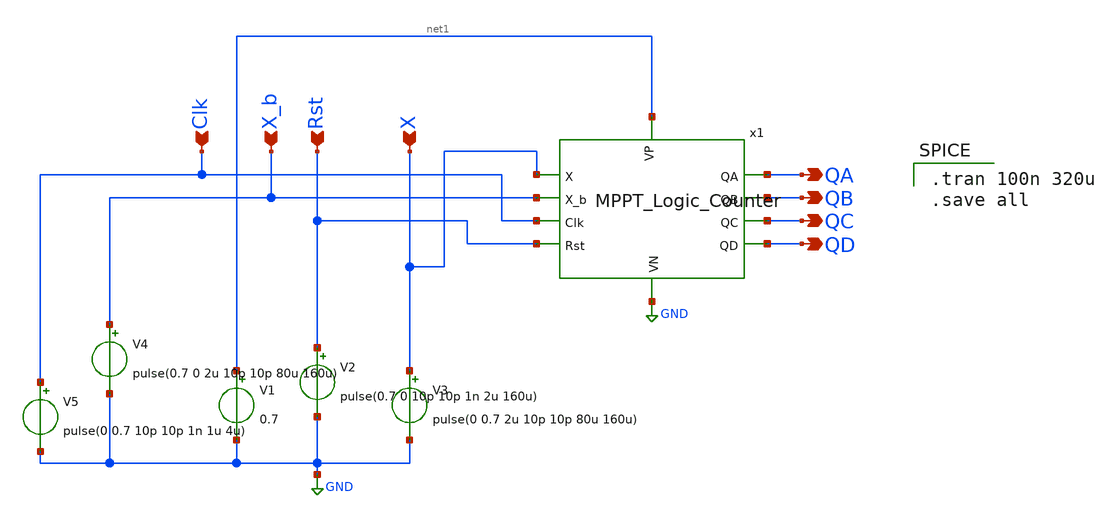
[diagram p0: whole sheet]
** sch_path: Blocks/MPPT/MPPT_Logic_Counter_test.sch
**.subckt MPPT_Logic_Counter_test QA Clk X_b Rst X QD QC QB
*.opin QA
*.ipin Clk
*.ipin X_b
*.ipin Rst
*.ipin X
*.opin QD
*.opin QC
*.opin QB
V2 Rst GND pulse(0.7 0 10p 10p 1n 2u 160u)
V4 X_b GND pulse(0.7 0 2u 10p 10p 80u 160u)
V5 Clk GND pulse(0 0.7 10p 10p 1n 1u 4u)
V3 X GND pulse(0 0.7 2u 10p 10p 80u 160u)
V1 net1 GND 0.7
x1 QA Clk X_b Rst GND X net1 QD QB QC MPPT_Logic_Counter
**** begin user architecture code

** opencircuitdesign pdks install
.lib $::SKYWATER_MODELS/sky130.lib.spice tt



.tran 100n 320u
.save all

**** end user architecture code
**.ends

* expanding   symbol:  pico_chipathon/Blocks/MPPT/MPPT_Logic_Counter.sym # of pins=10
** sym_path: Blocks/MPPT/MPPT_Logic_Counter.sym
** sch_path: Blocks/MPPT/MPPT_Logic_Counter.sch
.subckt MPPT_Logic_Counter QA Clk X_b Rst VN X VP QD QB QC
*.opin QD
*.ipin VP
*.opin QC
*.opin QB
*.opin QA
*.ipin VN
*.ipin X
*.ipin X_b
*.ipin Clk
*.ipin Rst
x4 net47 net46 net2 VP VN NAND
x5 QD X_b net38 VP VN NAND
x6 net51 net50 net3 VP VN NAND
x16 QA QD net29 VP VN NAND
x48 QB QD net31 VP VN NAND
x49 QC QD net32 VP VN NAND
x50 QD X net35 VP VN NAND
x52 net44 net43 net28 VP VN NAND
x54 VP net14 X_b QC QB_b QA_b VN nand4
x12 VP net15 X_b QD QB_b QA_b VN nand4
x15 VP net17 QD QC QB QA VN nand4
x22 VP net8 X QC_b QB QA VN nand4
x24 VP net36 X QC QB QA VN nand4
x17 VP net52 net53 net57 net50 VN nor3
x26 VP net54 net55 net56 net51 VN nor3
x56 VP net10 net11 net48 net46 VN nor3
x57 VP net49 net16 net18 net47 VN nor3
x25 VP net30 net33 net45 net43 VN nor3
x64 X_b QB QA VP VN net9 NAND3
x9 X QB_b QA VP VN net12 NAND3
x10 X QB QA_b VP VN net13 NAND3
x11 X_b QC QA VP VN net4 NAND3
x13 QC QB QA_b VP VN net5 NAND3
x14 QD QC QA VP VN net6 NAND3
x19 X QC QB_b VP VN net7 NAND3
x20 QC_b QB_b QA_b VP VN net39 NAND3
x23 VP net34 net37 net44 VN NOR2
x8 VP net38 net39 net56 VN NOR2
x1 net2 Clk Rst VN VP QB QB_b DFF1
x18 net3 Clk Rst VN VP QC QC_b DFF1
x29 net28 Clk Rst VN VP QD DFF
x32 net17 net18 VP VN INV
x38 net15 net16 VP VN INV
x39 net14 net49 VP VN INV
x40 net13 net48 VP VN INV
x42 net9 net10 VP VN INV
x43 net12 net11 VP VN INV
x31 net8 net55 VP VN INV
x33 net7 net54 VP VN INV
x36 net6 net57 VP VN INV
x37 net5 net53 VP VN INV
x41 net4 net52 VP VN INV
x34 net29 net30 VP VN INV
x44 net31 net33 VP VN INV
x51 net32 net45 VP VN INV
x53 net35 net34 VP VN INV
x55 net36 net37 VP VN INV
x35 net1 Clk Rst VN VP QA QA_b DFF1
x58 VP net20 net23 net42 net40 VN nor3
x59 VP net40 net41 net1 VN NOR2
x3 net27 net24 net41 VP VN NAND
x21 net19 net20 VP VN INV
x27 net21 net23 VP VN INV
x28 net22 net42 VP VN INV
x30 net25 net24 VP VN INV
x2 net26 net27 VP VN INV
x60 VP net26 X QD QC QB VN nand4
x7 QA_b QB net19 VP VN NAND
x45 QA_b QC net21 VP VN NAND
x46 QA_b QD net22 VP VN NAND
x47 QA_b X net25 VP VN NAND
.ends


* expanding   symbol:  pico_chipathon/component/NAND2/NAND.sym # of pins=5
** sym_path: component/NAND2/NAND.sym
** sch_path: component/NAND2/NAND.sch
.subckt NAND B A Y VP VN
*.iopin VP
*.ipin A
*.ipin B
*.opin Y
*.iopin VN
XM1 Y A VP VP sky130_fd_pr__pfet_01v8 L=0.15 W=1.26 nf=1 ad='int((nf+1)/2) * W/nf * 0.29' as='int((nf+2)/2) * W/nf * 0.29'
+ pd='2*int((nf+1)/2) * (W/nf + 0.29)' ps='2*int((nf+2)/2) * (W/nf + 0.29)' nrd='0.29 / W' nrs='0.29 / W'
+ sa=0 sb=0 sd=0 mult=1 m=1
XM2 Y B VP VP sky130_fd_pr__pfet_01v8 L=0.15 W=1.26 nf=1 ad='int((nf+1)/2) * W/nf * 0.29' as='int((nf+2)/2) * W/nf * 0.29'
+ pd='2*int((nf+1)/2) * (W/nf + 0.29)' ps='2*int((nf+2)/2) * (W/nf + 0.29)' nrd='0.29 / W' nrs='0.29 / W'
+ sa=0 sb=0 sd=0 mult=1 m=1
XM3 Y A net1 net1 sky130_fd_pr__nfet_01v8 L=0.15 W=0.84 nf=1 ad='int((nf+1)/2) * W/nf * 0.29' as='int((nf+2)/2) * W/nf * 0.29'
+ pd='2*int((nf+1)/2) * (W/nf + 0.29)' ps='2*int((nf+2)/2) * (W/nf + 0.29)' nrd='0.29 / W' nrs='0.29 / W'
+ sa=0 sb=0 sd=0 mult=1 m=1
XM4 net1 B VN VN sky130_fd_pr__nfet_01v8 L=0.15 W=0.84 nf=1 ad='int((nf+1)/2) * W/nf * 0.29' as='int((nf+2)/2) * W/nf * 0.29'
+ pd='2*int((nf+1)/2) * (W/nf + 0.29)' ps='2*int((nf+2)/2) * (W/nf + 0.29)' nrd='0.29 / W' nrs='0.29 / W'
+ sa=0 sb=0 sd=0 mult=1 m=1
.ends


* expanding   symbol:  pico_chipathon/component/NAND4/nand4.sym # of pins=7
** sym_path: component/NAND4/nand4.sym
** sch_path: component/NAND4/nand4.sch
.subckt nand4 VP Y A B C D VN
*.ipin A
*.ipin B
*.ipin C
*.opin Y
*.ipin D
*.ipin VP
*.ipin VN
XM1 Y A net1 VN sky130_fd_pr__nfet_01v8 L=0.15 W=1.68 nf=1 ad='int((nf+1)/2) * W/nf * 0.29' as='int((nf+2)/2) * W/nf * 0.29'
+ pd='2*int((nf+1)/2) * (W/nf + 0.29)' ps='2*int((nf+2)/2) * (W/nf + 0.29)' nrd='0.29 / W' nrs='0.29 / W'
+ sa=0 sb=0 sd=0 mult=1 m=1
XM2 net1 B net2 VN sky130_fd_pr__nfet_01v8 L=0.15 W=1.68 nf=1 ad='int((nf+1)/2) * W/nf * 0.29' as='int((nf+2)/2) * W/nf * 0.29'
+ pd='2*int((nf+1)/2) * (W/nf + 0.29)' ps='2*int((nf+2)/2) * (W/nf + 0.29)' nrd='0.29 / W' nrs='0.29 / W'
+ sa=0 sb=0 sd=0 mult=1 m=1
XM3 net2 C net3 VN sky130_fd_pr__nfet_01v8 L=0.15 W=1.68 nf=1 ad='int((nf+1)/2) * W/nf * 0.29' as='int((nf+2)/2) * W/nf * 0.29'
+ pd='2*int((nf+1)/2) * (W/nf + 0.29)' ps='2*int((nf+2)/2) * (W/nf + 0.29)' nrd='0.29 / W' nrs='0.29 / W'
+ sa=0 sb=0 sd=0 mult=1 m=1
XM4 Y A VP VP sky130_fd_pr__pfet_01v8 L=0.15 W=1.26 nf=1 ad='int((nf+1)/2) * W/nf * 0.29' as='int((nf+2)/2) * W/nf * 0.29'
+ pd='2*int((nf+1)/2) * (W/nf + 0.29)' ps='2*int((nf+2)/2) * (W/nf + 0.29)' nrd='0.29 / W' nrs='0.29 / W'
+ sa=0 sb=0 sd=0 mult=1 m=1
XM5 Y B VP VP sky130_fd_pr__pfet_01v8 L=0.15 W=1.26 nf=1 ad='int((nf+1)/2) * W/nf * 0.29' as='int((nf+2)/2) * W/nf * 0.29'
+ pd='2*int((nf+1)/2) * (W/nf + 0.29)' ps='2*int((nf+2)/2) * (W/nf + 0.29)' nrd='0.29 / W' nrs='0.29 / W'
+ sa=0 sb=0 sd=0 mult=1 m=1
XM6 Y C VP VP sky130_fd_pr__pfet_01v8 L=0.15 W=1.26 nf=1 ad='int((nf+1)/2) * W/nf * 0.29' as='int((nf+2)/2) * W/nf * 0.29'
+ pd='2*int((nf+1)/2) * (W/nf + 0.29)' ps='2*int((nf+2)/2) * (W/nf + 0.29)' nrd='0.29 / W' nrs='0.29 / W'
+ sa=0 sb=0 sd=0 mult=1 m=1
XM7 Y D VP VP sky130_fd_pr__pfet_01v8 L=0.15 W=1.26 nf=1 ad='int((nf+1)/2) * W/nf * 0.29' as='int((nf+2)/2) * W/nf * 0.29'
+ pd='2*int((nf+1)/2) * (W/nf + 0.29)' ps='2*int((nf+2)/2) * (W/nf + 0.29)' nrd='0.29 / W' nrs='0.29 / W'
+ sa=0 sb=0 sd=0 mult=1 m=1
XM8 net3 D VN VN sky130_fd_pr__nfet_01v8 L=0.15 W=1.68 nf=1 ad='int((nf+1)/2) * W/nf * 0.29' as='int((nf+2)/2) * W/nf * 0.29'
+ pd='2*int((nf+1)/2) * (W/nf + 0.29)' ps='2*int((nf+2)/2) * (W/nf + 0.29)' nrd='0.29 / W' nrs='0.29 / W'
+ sa=0 sb=0 sd=0 mult=1 m=1
.ends


* expanding   symbol:  pico_chipathon/component/NOR3/nor3.sym # of pins=6
** sym_path: component/NOR3/nor3.sym
** sch_path: component/NOR3/nor3.sch
.subckt nor3 VP A B C Y VN
*.opin Y
*.ipin C
*.ipin A
*.ipin B
*.ipin VP
*.ipin VN
XM5 Y B VN VN sky130_fd_pr__nfet_01v8 L=0.15 W=0.42 nf=1 ad='int((nf+1)/2) * W/nf * 0.29' as='int((nf+2)/2) * W/nf * 0.29'
+ pd='2*int((nf+1)/2) * (W/nf + 0.29)' ps='2*int((nf+2)/2) * (W/nf + 0.29)' nrd='0.29 / W' nrs='0.29 / W'
+ sa=0 sb=0 sd=0 mult=1 m=1
XM3 Y A VN VN sky130_fd_pr__nfet_01v8 L=0.15 W=0.42 nf=1 ad='int((nf+1)/2) * W/nf * 0.29' as='int((nf+2)/2) * W/nf * 0.29'
+ pd='2*int((nf+1)/2) * (W/nf + 0.29)' ps='2*int((nf+2)/2) * (W/nf + 0.29)' nrd='0.29 / W' nrs='0.29 / W'
+ sa=0 sb=0 sd=0 mult=1 m=1
XM2 Y C net2 VP sky130_fd_pr__pfet_01v8 L=0.15 W=3.78 nf=1 ad='int((nf+1)/2) * W/nf * 0.29' as='int((nf+2)/2) * W/nf * 0.29'
+ pd='2*int((nf+1)/2) * (W/nf + 0.29)' ps='2*int((nf+2)/2) * (W/nf + 0.29)' nrd='0.29 / W' nrs='0.29 / W'
+ sa=0 sb=0 sd=0 mult=1 m=1
XM1 net1 A VP VP sky130_fd_pr__pfet_01v8 L=0.15 W=3.78 nf=1 ad='int((nf+1)/2) * W/nf * 0.29' as='int((nf+2)/2) * W/nf * 0.29'
+ pd='2*int((nf+1)/2) * (W/nf + 0.29)' ps='2*int((nf+2)/2) * (W/nf + 0.29)' nrd='0.29 / W' nrs='0.29 / W'
+ sa=0 sb=0 sd=0 mult=1 m=1
XM6 net2 B net1 VP sky130_fd_pr__pfet_01v8 L=0.15 W=3.78 nf=1 ad='int((nf+1)/2) * W/nf * 0.29' as='int((nf+2)/2) * W/nf * 0.29'
+ pd='2*int((nf+1)/2) * (W/nf + 0.29)' ps='2*int((nf+2)/2) * (W/nf + 0.29)' nrd='0.29 / W' nrs='0.29 / W'
+ sa=0 sb=0 sd=0 mult=1 m=1
XM8 Y C VN VN sky130_fd_pr__nfet_01v8 L=0.15 W=0.42 nf=1 ad='int((nf+1)/2) * W/nf * 0.29' as='int((nf+2)/2) * W/nf * 0.29'
+ pd='2*int((nf+1)/2) * (W/nf + 0.29)' ps='2*int((nf+2)/2) * (W/nf + 0.29)' nrd='0.29 / W' nrs='0.29 / W'
+ sa=0 sb=0 sd=0 mult=1 m=1
.ends


* expanding   symbol:  pico_chipathon/component/NAND3/NAND3.sym # of pins=6
** sym_path: component/NAND3/NAND3.sym
** sch_path: component/NAND3/NAND3.sch
.subckt NAND3 A B C VP VN Y
*.iopin VP
*.iopin VN
*.ipin A
*.ipin B
*.ipin C
*.opin Y
XM1 Y A net1 VN sky130_fd_pr__nfet_01v8 L=0.15 W=1.26 nf=1 ad='int((nf+1)/2) * W/nf * 0.29' as='int((nf+2)/2) * W/nf * 0.29'
+ pd='2*int((nf+1)/2) * (W/nf + 0.29)' ps='2*int((nf+2)/2) * (W/nf + 0.29)' nrd='0.29 / W' nrs='0.29 / W'
+ sa=0 sb=0 sd=0 mult=1 m=1
XM2 net1 B net2 VN sky130_fd_pr__nfet_01v8 L=0.15 W=1.26 nf=1 ad='int((nf+1)/2) * W/nf * 0.29' as='int((nf+2)/2) * W/nf * 0.29'
+ pd='2*int((nf+1)/2) * (W/nf + 0.29)' ps='2*int((nf+2)/2) * (W/nf + 0.29)' nrd='0.29 / W' nrs='0.29 / W'
+ sa=0 sb=0 sd=0 mult=1 m=1
XM3 net2 C VN VN sky130_fd_pr__nfet_01v8 L=0.15 W=1.26 nf=1 ad='int((nf+1)/2) * W/nf * 0.29' as='int((nf+2)/2) * W/nf * 0.29'
+ pd='2*int((nf+1)/2) * (W/nf + 0.29)' ps='2*int((nf+2)/2) * (W/nf + 0.29)' nrd='0.29 / W' nrs='0.29 / W'
+ sa=0 sb=0 sd=0 mult=1 m=1
XM4 Y A VP VP sky130_fd_pr__pfet_01v8 L=0.15 W=1.26 nf=1 ad='int((nf+1)/2) * W/nf * 0.29' as='int((nf+2)/2) * W/nf * 0.29'
+ pd='2*int((nf+1)/2) * (W/nf + 0.29)' ps='2*int((nf+2)/2) * (W/nf + 0.29)' nrd='0.29 / W' nrs='0.29 / W'
+ sa=0 sb=0 sd=0 mult=1 m=1
XM5 Y B VP VP sky130_fd_pr__pfet_01v8 L=0.15 W=1.26 nf=1 ad='int((nf+1)/2) * W/nf * 0.29' as='int((nf+2)/2) * W/nf * 0.29'
+ pd='2*int((nf+1)/2) * (W/nf + 0.29)' ps='2*int((nf+2)/2) * (W/nf + 0.29)' nrd='0.29 / W' nrs='0.29 / W'
+ sa=0 sb=0 sd=0 mult=1 m=1
XM6 Y C VP VP sky130_fd_pr__pfet_01v8 L=0.15 W=1.26 nf=1 ad='int((nf+1)/2) * W/nf * 0.29' as='int((nf+2)/2) * W/nf * 0.29'
+ pd='2*int((nf+1)/2) * (W/nf + 0.29)' ps='2*int((nf+2)/2) * (W/nf + 0.29)' nrd='0.29 / W' nrs='0.29 / W'
+ sa=0 sb=0 sd=0 mult=1 m=1
.ends


* expanding   symbol:  pico_chipathon/component/NOR2/NOR2.sym # of pins=5
** sym_path: component/NOR2/NOR2.sym
** sch_path: component/NOR2/NOR2.sch
.subckt NOR2 VP A B Y VN
*.opin Y
*.ipin A
*.ipin B
*.ipin VP
*.ipin VN
XM5 Y B VN VN sky130_fd_pr__nfet_01v8 L=0.15 W=0.42 nf=1 ad='int((nf+1)/2) * W/nf * 0.29' as='int((nf+2)/2) * W/nf * 0.29'
+ pd='2*int((nf+1)/2) * (W/nf + 0.29)' ps='2*int((nf+2)/2) * (W/nf + 0.29)' nrd='0.29 / W' nrs='0.29 / W'
+ sa=0 sb=0 sd=0 mult=1 m=1
XM3 Y A VN VN sky130_fd_pr__nfet_01v8 L=0.15 W=0.42 nf=1 ad='int((nf+1)/2) * W/nf * 0.29' as='int((nf+2)/2) * W/nf * 0.29'
+ pd='2*int((nf+1)/2) * (W/nf + 0.29)' ps='2*int((nf+2)/2) * (W/nf + 0.29)' nrd='0.29 / W' nrs='0.29 / W'
+ sa=0 sb=0 sd=0 mult=1 m=1
XM2 net1 A VP VP sky130_fd_pr__pfet_01v8 L=0.15 W=2.52 nf=1 ad='int((nf+1)/2) * W/nf * 0.29' as='int((nf+2)/2) * W/nf * 0.29'
+ pd='2*int((nf+1)/2) * (W/nf + 0.29)' ps='2*int((nf+2)/2) * (W/nf + 0.29)' nrd='0.29 / W' nrs='0.29 / W'
+ sa=0 sb=0 sd=0 mult=1 m=1
XM4 Y B net1 VP sky130_fd_pr__pfet_01v8 L=0.15 W=2.52 nf=1 ad='int((nf+1)/2) * W/nf * 0.29' as='int((nf+2)/2) * W/nf * 0.29'
+ pd='2*int((nf+1)/2) * (W/nf + 0.29)' ps='2*int((nf+2)/2) * (W/nf + 0.29)' nrd='0.29 / W' nrs='0.29 / W'
+ sa=0 sb=0 sd=0 mult=1 m=1
.ends


* expanding   symbol:  pico_chipathon/component/FlipFlops/DFF1.sym # of pins=7
** sym_path: component/FlipFlops/DFF1.sym
** sch_path: component/FlipFlops/DFF1.sch
.subckt DFF1 D Clk RST VN VP Q Qb
*.opin Q
*.iopin VN
*.iopin VP
*.ipin Clk
*.ipin D
*.ipin RST
*.opin Qb
x7 net2 net4 net3 VP VN NAND
x8 net3 Clk RST VP VN net2 NAND3
x6 Q net1 RST VP VN Qb NAND3
x4 net2 Clk net4 VP VN net1 NAND3
x5 net1 D RST VP VN net4 NAND3
x1 Qb net2 Q VP VN NAND
.ends


* expanding   symbol:  pico_chipathon/component/FlipFlops/DFF.sym # of pins=6
** sym_path: component/FlipFlops/DFF.sym
** sch_path: component/FlipFlops/DFF.sch
.subckt DFF D Clk RST VN VP Q
*.opin Q
*.iopin VN
*.iopin VP
*.ipin Clk
*.ipin D
*.ipin RST
x1 net2 net5 net4 VP VN NAND
x7 net4 Clk RST VP VN net2 NAND3
x3 Q net1 RST VP VN net3 NAND3
x4 net2 Clk net5 VP VN net1 NAND3
x5 net1 D RST VP VN net5 NAND3
x6 net3 net2 Q VP VN NAND
.ends


* expanding   symbol:  pico_chipathon/component/INV/INV.sym # of pins=4
** sym_path: component/INV/INV.sym
** sch_path: component/INV/INV.sch
.subckt INV X Y VP VN
*.ipin X
*.opin Y
*.iopin VN
*.iopin VP
XM1 Y X VN VN sky130_fd_pr__nfet_01v8 L=0.15 W=0.42 nf=1 ad='int((nf+1)/2) * W/nf * 0.29' as='int((nf+2)/2) * W/nf * 0.29'
+ pd='2*int((nf+1)/2) * (W/nf + 0.29)' ps='2*int((nf+2)/2) * (W/nf + 0.29)' nrd='0.29 / W' nrs='0.29 / W'
+ sa=0 sb=0 sd=0 mult=1 m=1
XM2 Y X VP VP sky130_fd_pr__pfet_01v8 L=0.15 W=1.26 nf=1 ad='int((nf+1)/2) * W/nf * 0.29' as='int((nf+2)/2) * W/nf * 0.29'
+ pd='2*int((nf+1)/2) * (W/nf + 0.29)' ps='2*int((nf+2)/2) * (W/nf + 0.29)' nrd='0.29 / W' nrs='0.29 / W'
+ sa=0 sb=0 sd=0 mult=1 m=1
.ends

.GLOBAL GND
.end
